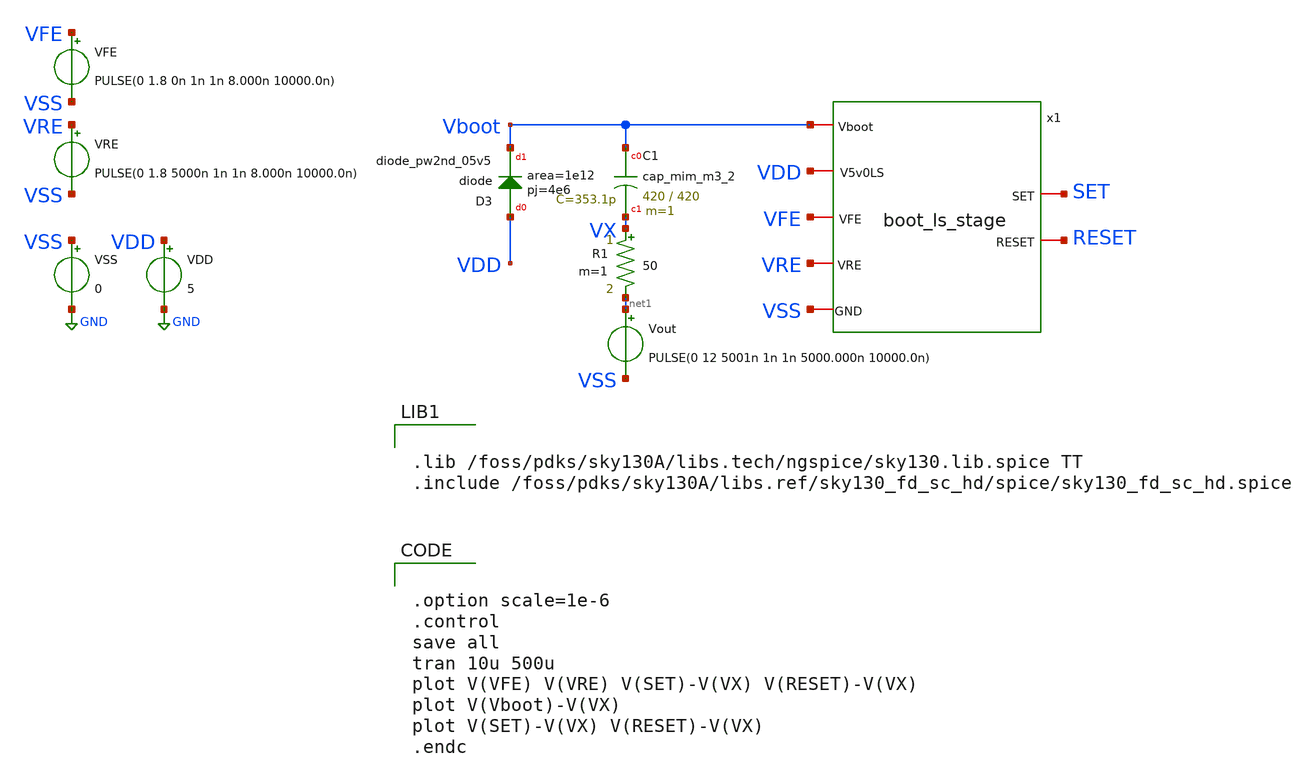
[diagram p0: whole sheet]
** sch_path: xschem/test/tb_boot_ls_stage.sch
**.subckt tb_boot_ls_stage
VDD VDD GND 5
VSS VSS GND 0
VRE VRE VSS PULSE(0 1.8 5000n 1n 1n 8.000n 10000.0n)
VFE VFE VSS PULSE(0 1.8 0n 1n 1n 8.000n 10000.0n)
XC1 Vboot VX sky130_fd_pr__cap_mim_m3_2 W=420 L=420 MF=1 m=1
XD3 VDD Vboot sky130_fd_pr__diode_pw2nd_05v5 area=1e12 pj=4e6
Vout net1 VSS PULSE(0 12 5001n 1n 1n 5000.000n 10000.0n)
R1 VX net1 50 m=1
x1 Vboot VDD SET RESET VSS VFE VRE boot_ls_stage
**** begin user architecture code


.lib /foss/pdks/sky130A/libs.tech/ngspice/sky130.lib.spice TT
.include /foss/pdks/sky130A/libs.ref/sky130_fd_sc_hd/spice/sky130_fd_sc_hd.spice




.option scale=1e-6
.control
save all
tran 10u 500u
plot V(VFE) V(VRE) V(SET)-V(VX) V(RESET)-V(VX)
plot V(Vboot)-V(VX)
plot V(SET)-V(VX) V(RESET)-V(VX)
.endc


**** end user architecture code
**.ends

* expanding   symbol:  /foss/designs/Open3LFCC_V2_GD12V/xschem/boot_ls_stage.sym # of pins=7
** sym_path: xschem/boot_ls_stage.sym
** sch_path: xschem/boot_ls_stage.sch
.subckt boot_ls_stage Vboot V5v0LS SET RESET GND VFE VRE
*.iopin V5v0LS
*.iopin GND
*.iopin Vboot
*.iopin VFE
*.iopin VRE
*.iopin SET
*.iopin RESET
XM7 net1 RESET Vboot Vboot sky130_fd_pr__pfet_g5v0d10v5 L=0.5 W=1 nf=1 ad='int((nf+1)/2) * W/nf * 0.29'
+ as='int((nf+2)/2) * W/nf * 0.29' pd='2*int((nf+1)/2) * (W/nf + 0.29)' ps='2*int((nf+2)/2) * (W/nf + 0.29)'
+ nrd='0.29 / W' nrs='0.29 / W' sa=0 sb=0 sd=0 mult=1 m=1
XM8 SET SET net1 net1 sky130_fd_pr__pfet_g5v0d10v5 L=0.5 W=1 nf=1 ad='int((nf+1)/2) * W/nf * 0.29' as='int((nf+2)/2) * W/nf * 0.29'
+ pd='2*int((nf+1)/2) * (W/nf + 0.29)' ps='2*int((nf+2)/2) * (W/nf + 0.29)' nrd='0.29 / W' nrs='0.29 / W'
+ sa=0 sb=0 sd=0 mult=1 m=1
XM4 RESET SET Vboot Vboot sky130_fd_pr__pfet_g5v0d10v5 L=1 W=5 nf=1 ad='int((nf+1)/2) * W/nf * 0.29'
+ as='int((nf+2)/2) * W/nf * 0.29' pd='2*int((nf+1)/2) * (W/nf + 0.29)' ps='2*int((nf+2)/2) * (W/nf + 0.29)'
+ nrd='0.29 / W' nrs='0.29 / W' sa=0 sb=0 sd=0 mult=1 m=1
XM3 SET SET Vboot Vboot sky130_fd_pr__pfet_g5v0d10v5 L=1 W=0.5 nf=1 ad='int((nf+1)/2) * W/nf * 0.29'
+ as='int((nf+2)/2) * W/nf * 0.29' pd='2*int((nf+1)/2) * (W/nf + 0.29)' ps='2*int((nf+2)/2) * (W/nf + 0.29)'
+ nrd='0.29 / W' nrs='0.29 / W' sa=0 sb=0 sd=0 mult=1 m=1
XM9 net3 SET Vboot Vboot sky130_fd_pr__pfet_g5v0d10v5 L=1 W=0.5 nf=1 ad='int((nf+1)/2) * W/nf * 0.29'
+ as='int((nf+2)/2) * W/nf * 0.29' pd='2*int((nf+1)/2) * (W/nf + 0.29)' ps='2*int((nf+2)/2) * (W/nf + 0.29)'
+ nrd='0.29 / W' nrs='0.29 / W' sa=0 sb=0 sd=0 mult=1 m=1
XM10 RESET RESET net3 net3 sky130_fd_pr__pfet_g5v0d10v5 L=1 W=0.5 nf=1 ad='int((nf+1)/2) * W/nf * 0.29'
+ as='int((nf+2)/2) * W/nf * 0.29' pd='2*int((nf+1)/2) * (W/nf + 0.29)' ps='2*int((nf+2)/2) * (W/nf + 0.29)'
+ nrd='0.29 / W' nrs='0.29 / W' sa=0 sb=0 sd=0 mult=1 m=1
XM5 SET RESET Vboot Vboot sky130_fd_pr__pfet_g5v0d10v5 L=1 W=5 nf=1 ad='int((nf+1)/2) * W/nf * 0.29'
+ as='int((nf+2)/2) * W/nf * 0.29' pd='2*int((nf+1)/2) * (W/nf + 0.29)' ps='2*int((nf+2)/2) * (W/nf + 0.29)'
+ nrd='0.29 / W' nrs='0.29 / W' sa=0 sb=0 sd=0 mult=1 m=1
XM6 RESET RESET Vboot Vboot sky130_fd_pr__pfet_g5v0d10v5 L=1 W=0.5 nf=1 ad='int((nf+1)/2) * W/nf * 0.29'
+ as='int((nf+2)/2) * W/nf * 0.29' pd='2*int((nf+1)/2) * (W/nf + 0.29)' ps='2*int((nf+2)/2) * (W/nf + 0.29)'
+ nrd='0.29 / W' nrs='0.29 / W' sa=0 sb=0 sd=0 mult=1 m=1
I0 V5v0LS net4 30u
XM11 net4 net4 GND GND sky130_fd_pr__nfet_g5v0d10v5 L=2 W=4 nf=1 ad='int((nf+1)/2) * W/nf * 0.29' as='int((nf+2)/2) * W/nf * 0.29'
+ pd='2*int((nf+1)/2) * (W/nf + 0.29)' ps='2*int((nf+2)/2) * (W/nf + 0.29)' nrd='0.29 / W' nrs='0.29 / W'
+ sa=0 sb=0 sd=0 mult=1 m=1
XM12 net2 net4 GND GND sky130_fd_pr__nfet_g5v0d10v5 L=2 W=8 nf=1 ad='int((nf+1)/2) * W/nf * 0.29' as='int((nf+2)/2) * W/nf * 0.29'
+ pd='2*int((nf+1)/2) * (W/nf + 0.29)' ps='2*int((nf+2)/2) * (W/nf + 0.29)' nrd='0.29 / W' nrs='0.29 / W'
+ sa=0 sb=0 sd=0 mult=1 m=1
XM19 SET VRE net2 net2 sky130_fd_pr__nfet_g5v0d10v5 L=0.5 W=6 nf=1 ad='int((nf+1)/2) * W/nf * 0.29' as='int((nf+2)/2) * W/nf * 0.29'
+ pd='2*int((nf+1)/2) * (W/nf + 0.29)' ps='2*int((nf+2)/2) * (W/nf + 0.29)' nrd='0.29 / W' nrs='0.29 / W'
+ sa=0 sb=0 sd=0 mult=1 m=1
XM1 RESET VFE net2 net2 sky130_fd_pr__nfet_g5v0d10v5 L=0.5 W=6 nf=1 ad='int((nf+1)/2) * W/nf * 0.29'
+ as='int((nf+2)/2) * W/nf * 0.29' pd='2*int((nf+1)/2) * (W/nf + 0.29)' ps='2*int((nf+2)/2) * (W/nf + 0.29)'
+ nrd='0.29 / W' nrs='0.29 / W' sa=0 sb=0 sd=0 mult=1 m=1
.ends

.GLOBAL GND
.end
